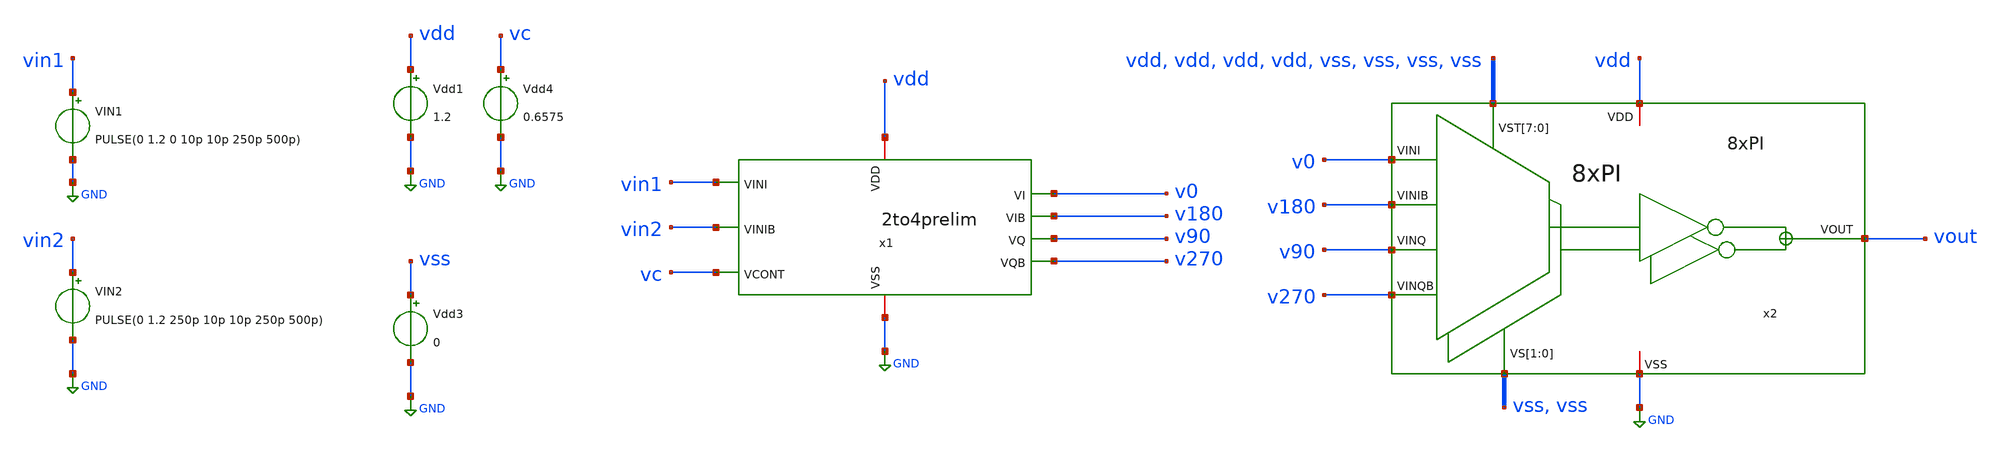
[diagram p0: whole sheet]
** sch_path: 2to4/tb_2to4prelim.sch
**.subckt tb_2to4prelim
Vdd1 vdd GND 1.2
VIN1 vin1 GND PULSE(0 1.2 0 10p 10p 250p 500p)
VIN2 vin2 GND PULSE(0 1.2 250p 10p 10p 250p 500p)
x1 vdd v270 v90 vin1 GND vc v180 v0 vin2 2to4prelim
Vdd4 vc GND 0.6575
x2 v0 v180 v90 v270 vss vss vdd vdd vdd vdd vss vss vss vss vout vdd GND 8xPI
Vdd3 vss GND 0
**** begin user architecture code

.lib cornerMOSlv.lib mos_tt
.include /foss/pdks/ihp-sg13g2/libs.ref/sg13g2_stdcell/spice/sg13g2_stdcell.spice




.save v(vin1) v(v0) v(v90) v(v270) v(v180) v(vin2) v(vout)

* CAMBIO CRITICO: 1p en vez de 10p para que el 'meas' encuentre los cruces
.tran 1p 3n
.save all

.control
run
set color0=white
write tran_logic.raw

* --- MEDICIONES DE FASE Y RETARDO (Usando v90) ---
* Periodo Entrada (Ref)
meas tran T_p90 TRIG v(v0) VAL=0.6 RISE=3 TARG v(v0) VAL=0.6 RISE=4

* Retardo (Entrada vs v90)
meas tran T_d90 TRIG v(v0) VAL=0.6 RISE=3 TARG v(v90) VAL=0.6 RISE=3

* Calculo Fase (Agregue espacios para que Ngspice no de error)
let Phase_D90 = ( T_d90 / T_p90 ) * 360

print T_p90
print T_d90
print Phase_D90

* --- DUTY CYCLE (Usando v90) ---
* Periodo Salida
meas tran T_pe90 TRIG v(v90) VAL=0.6 RISE=2 TARG v(v90) VAL=0.6 RISE=3

* Tiempo en ALTO (Ton)
meas tran T_h90 TRIG v(v90) VAL=0.6 RISE=2 TARG v(v90) VAL=0.6 FALL=2

* Tiempo en BAJO (Toff)
meas tran T_l90 TRIG v(v90) VAL=0.6 FALL=2 TARG v(v90) VAL=0.6 RISE=3

* Calculo Duty (Agregue espacios vitales)
let Duty_H90 = ( T_h90 / T_pe90 ) * 100
let Duty_L90 = ( T_l90 / T_pe90 ) * 100

print Duty_H90
print Duty_L90

.endc


**** end user architecture code
**.ends
.GLOBAL GND
.end
